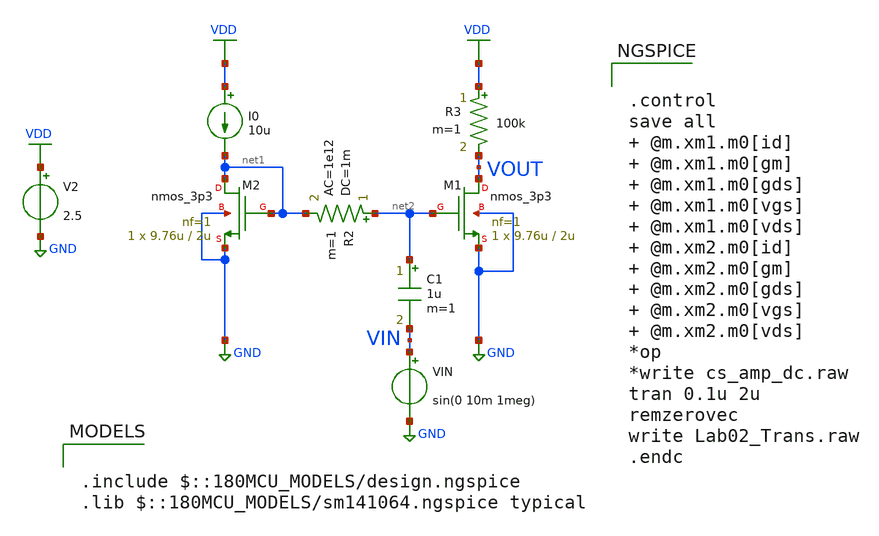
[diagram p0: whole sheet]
** sch_path: ITI_Labs/Lab2/Design/Lab02_Trans.sch
**.subckt Lab02_Trans
XM1 VOUT net2 GND GND nmos_3p3 L=2u W=9.76u nf=1 ad='int((nf+1)/2) * W/nf * 0.18u' as='int((nf+2)/2) * W/nf * 0.18u'
+ pd='2*int((nf+1)/2) * (W/nf + 0.18u)' ps='2*int((nf+2)/2) * (W/nf + 0.18u)' nrd='0.18u / W' nrs='0.18u / W'
+ sa=0 sb=0 sd=0 m=1
XM2 net1 net1 GND GND nmos_3p3 L=2u W=9.76u nf=1 ad='int((nf+1)/2) * W/nf * 0.18u' as='int((nf+2)/2) * W/nf * 0.18u'
+ pd='2*int((nf+1)/2) * (W/nf + 0.18u)' ps='2*int((nf+2)/2) * (W/nf + 0.18u)' nrd='0.18u / W' nrs='0.18u / W'
+ sa=0 sb=0 sd=0 m=1
R2 net2 net1 1m ac=1e12 m=1
I0 VDD net1 10u
VIN VIN GND sin(0 10m 1meg)
V2 VDD GND 2.5
R3 VDD VOUT 100k m=1
C1 net2 VIN 1u m=1
**** begin user architecture code

.include $::180MCU_MODELS/design.ngspice
.lib $::180MCU_MODELS/sm141064.ngspice typical



.control
save all  @m.xm1.m0[id]  @m.xm1.m0[gm]  @m.xm1.m0[gds]  @m.xm1.m0[vgs]  @m.xm1.m0[vds]
+  @m.xm2.m0[id]  @m.xm2.m0[gm]  @m.xm2.m0[gds]  @m.xm2.m0[vgs]  @m.xm2.m0[vds]
*op
*write cs_amp_dc.raw
tran 0.1u 2u
remzerovec
write Lab02_Trans.raw
.endc


**** end user architecture code
**.ends
.GLOBAL GND
.GLOBAL VDD
.end
